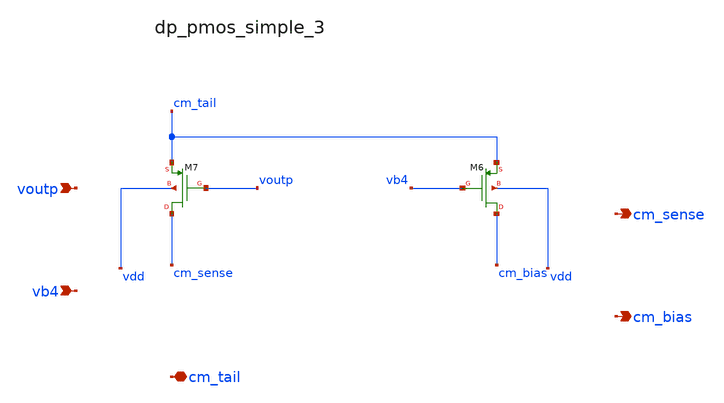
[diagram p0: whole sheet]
** sch_path: analog-db/raw/amp_027_fan_rrl_ota/hier/blocks/dp_pmos_simple_3.sch
**.subckt dp_pmos_simple_3 voutp vb4 cm_tail cm_sense cm_bias
*.ipin voutp
*.ipin vb4
*.iopin cm_tail
*.opin cm_sense
*.opin cm_bias
XM6 cm_bias vb4 cm_tail vdd sg13_lv_pmos w=x_dut_xm6_w l=x_dut_xm6_l ng=1 m=x_dut_xm6_m
XM7 cm_sense voutp cm_tail vdd sg13_lv_pmos w=x_dut_xm7_w l=x_dut_xm7_l ng=1 m=x_dut_xm7_m
**.ends
.end
